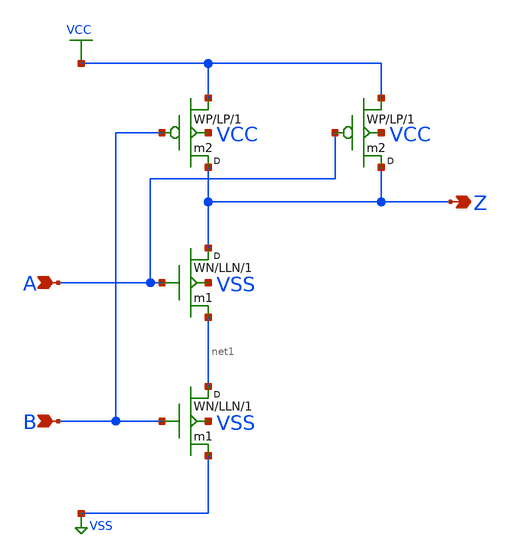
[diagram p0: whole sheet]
** sch_path: xschem_libraries_oa/examples/nand2/schematic/nand2.sch
* Copyright (C) 1998-2024 Stefan Frederik Schippers
* This program is free software; you can redistribute it and/or modify
* it under the terms of the GNU General Public License as published by
* the Free Software Foundation; either version 2 of the License, or
* (at your option) any later version.
* This program is distributed in the hope that it will be useful,
* but WITHOUT ANY WARRANTY; without even the implied warranty of
* MERCHANTABILITY or FITNESS FOR A PARTICULAR PURPOSE.  See the
* GNU General Public License for more details.
* You should have received a copy of the GNU General Public License
* along with this program; if not, write to the Free Software
**.subckt nand2 A Z B
*.ipin A
*.opin Z
*.ipin B
m1 Z A net1 VSS CMOSN w=WN l=LLN m=1
m1 net1 B VSS VSS CMOSN w=WN l=LLN m=1
m2 Z B VCC VCC CMOSP w=WP l=LP m=1
m2 Z A VCC VCC CMOSP w=WP l=LP m=1
**.ends
.GLOBAL VSS
.GLOBAL VCC
.end
